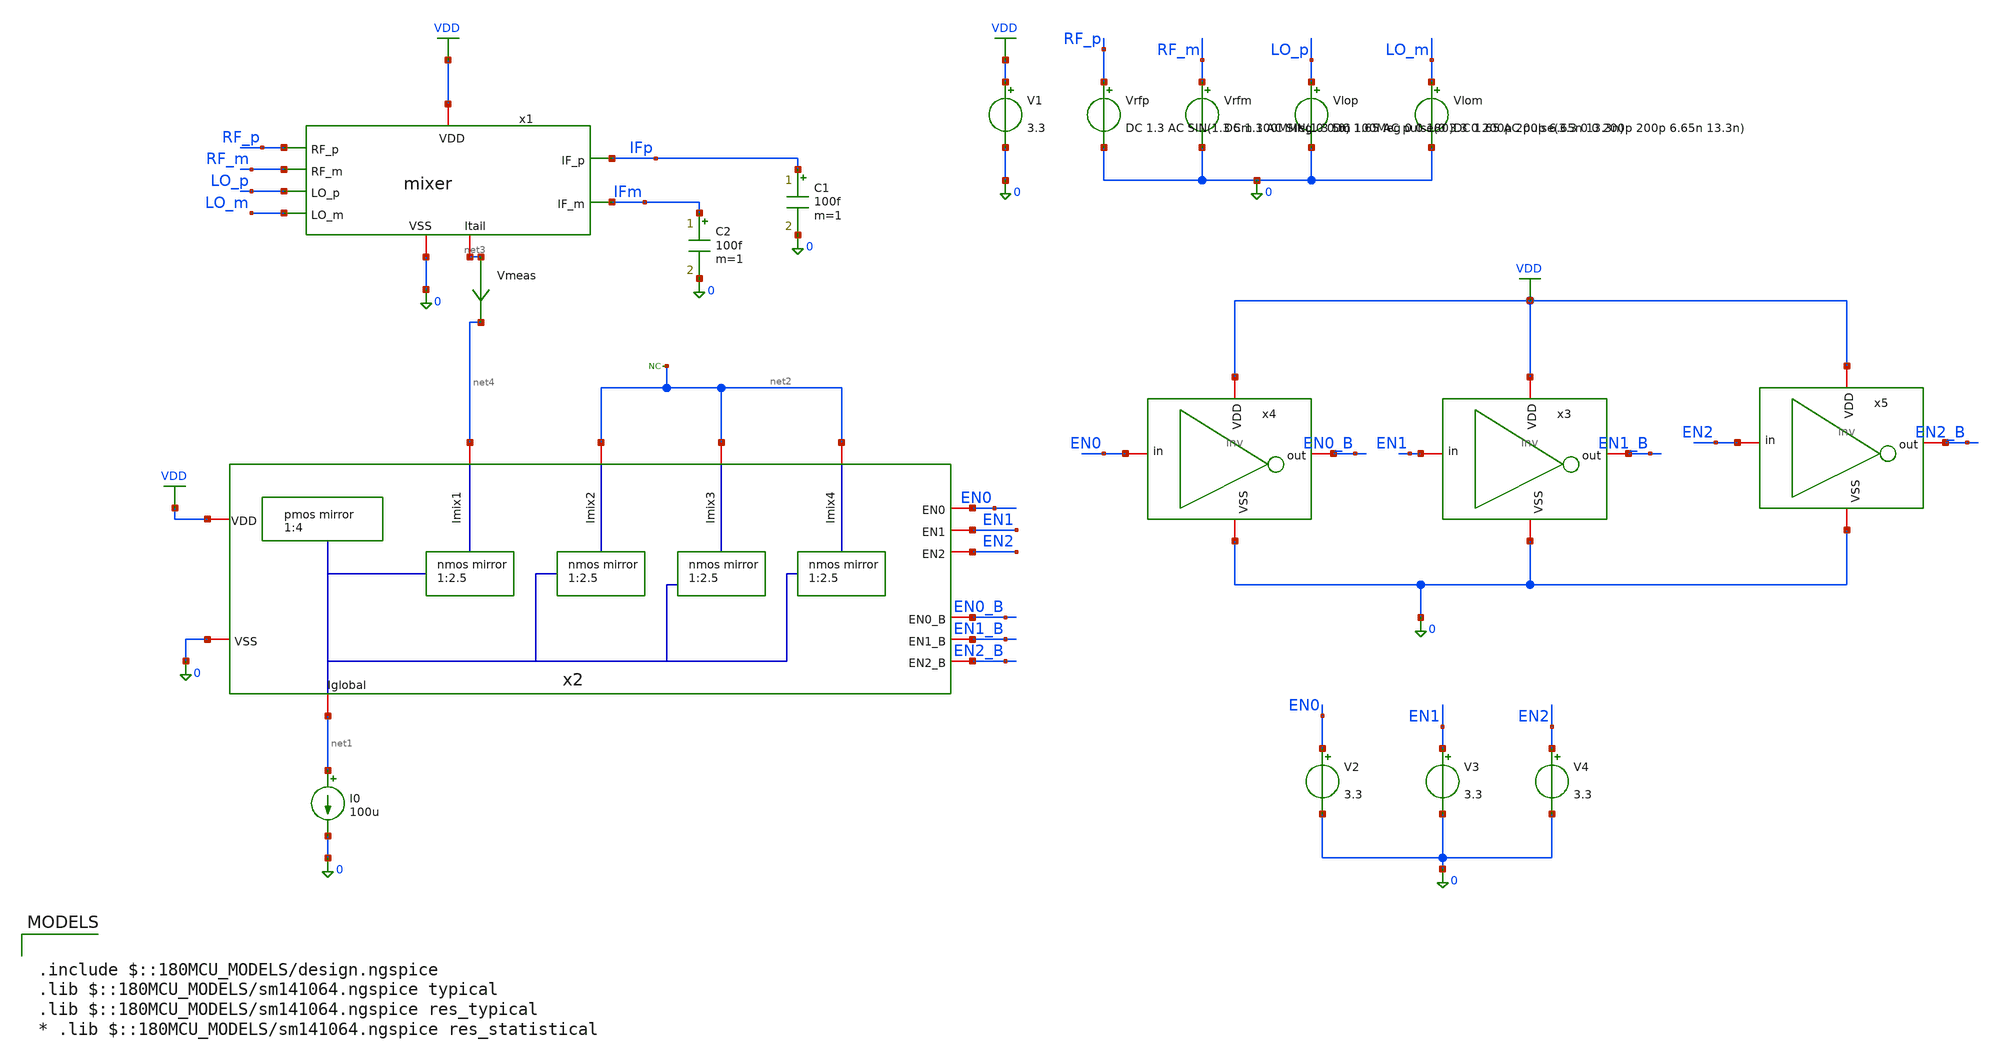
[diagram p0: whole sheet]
** sch_path: designs/mixer/testbench/mixer_with_mirror_en_tb.sch
**.subckt mixer_with_mirror_en_tb
V1 VDD 0 3.3
Vrfp RF_p 0 DC 1.3 AC SIN(1.3 5m 100MMeg 0 0 0)
Vrfm RF_m 0 DC 1.3 AC SIN(1.3 5m 100Meg 0 0 180)
Vlop LO_p 0 DC 1.65 AC pulse(0 3.3 0 200p 200p 6.65n 13.3n)
Vlom LO_m 0 DC 1.65 AC pulse(3.3 0 0 200p 200p 6.65n 13.3n)
C1 IFp 0 100f m=1
C2 IFm 0 100f m=1
I0 net1 0 100u
* noconn #net2
x1 IFp RF_p VDD 0 IFm RF_m LO_p net3 LO_m mixer
Vmeas net3 net4 0
.save i(vmeas)
x2 EN2 EN1 EN0 EN0_B EN1_B EN2_B VDD net1 net2 net4 0 net2 net2 mirror_network_with_enable
x3 VDD EN1_B EN1 0 inv
x4 VDD EN0_B EN0 0 inv
x5 VDD EN2_B EN2 0 inv
V2 EN0 0 3.3
V3 EN1 0 3.3
V4 EN2 0 3.3
**** begin user architecture code

.include $::180MCU_MODELS/design.ngspice
.lib $::180MCU_MODELS/sm141064.ngspice typical
.lib $::180MCU_MODELS/sm141064.ngspice res_typical
* .lib $::180MCU_MODELS/sm141064.ngspice res_statistical




.control

destroy all
save all
write mixer_tb.raw

op
echo RF pair
print @m.x1.xm1.m0[gm]
print @m.x1.xm1.m0[id]
print @m.x1.xm1.m0[vgs]
print @m.x1.xm1.m0[vds]
print @m.x1.xm1.m0[vdsat]

echo LO pair
print @m.x1.xm3.m0[gm]
print @m.x1.xm3.m0[id]
print @m.x1.xm3.m0[vgs]
print @m.x1.xm3.m0[vds]
print @m.x1.xm3.m0[vdsat]

echo nmos tail
print @m.x2.x2.xm2.m0[gm]
print @m.x2.x2.xm2.m0[id]
print @m.x2.x2.xm2.m0[vgs]
print @m.x2.x2.xm2.m0[vds]
print @m.x2.x2.xm2.m0[vdsat]

print i(vmeas)
tran 0.01n 2u ;transient sim
let vrf = V(RF_p)-V(RF_m)
let vif = V(IFp)-V(IFm)

plot V(LO_p)
plot vrf
plot vif

fft vif vrf

plot mag(vif) vs frequency
.endc


**** end user architecture code
**.ends
.GLOBAL VDD
.end
